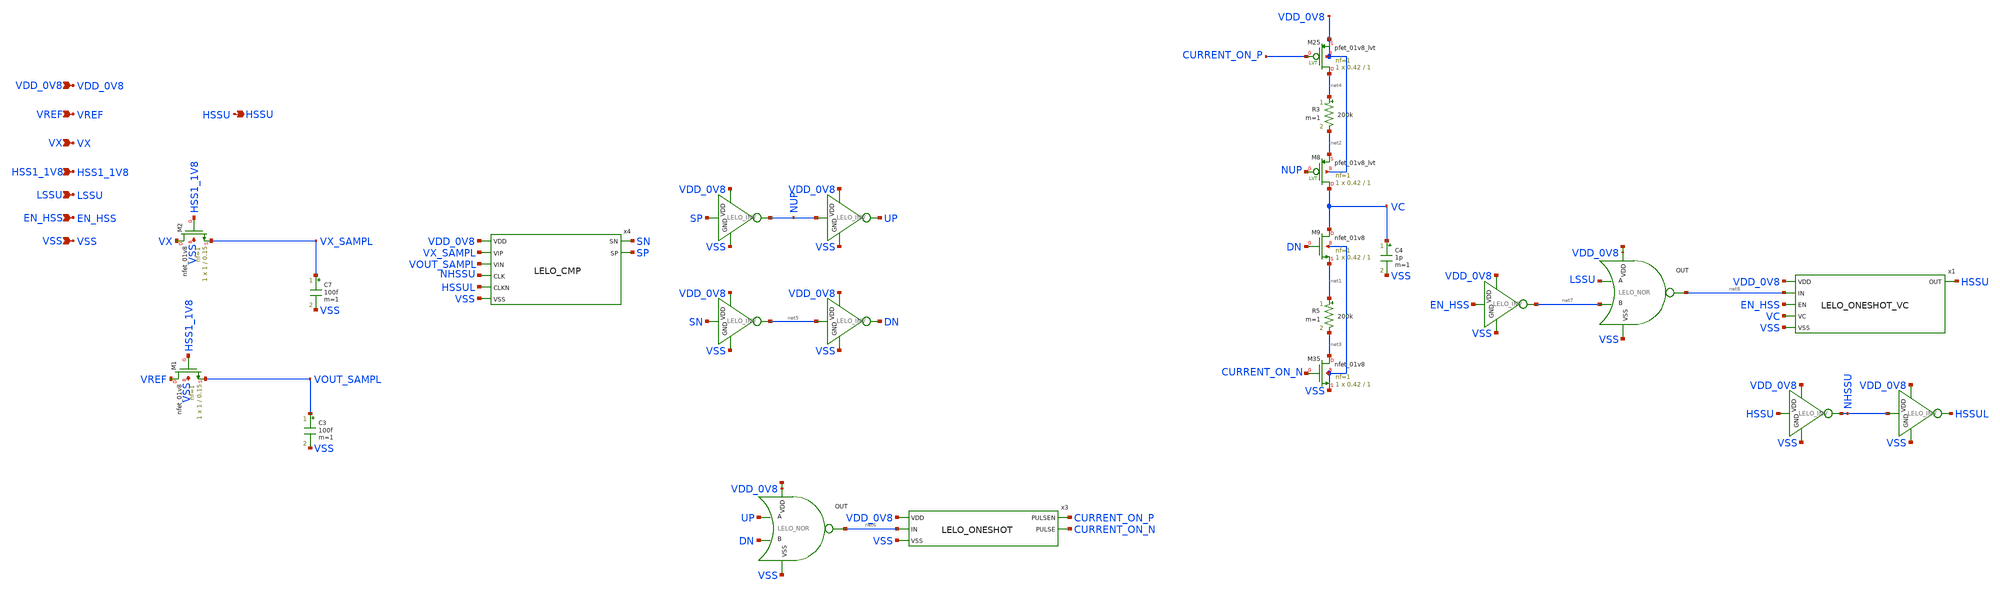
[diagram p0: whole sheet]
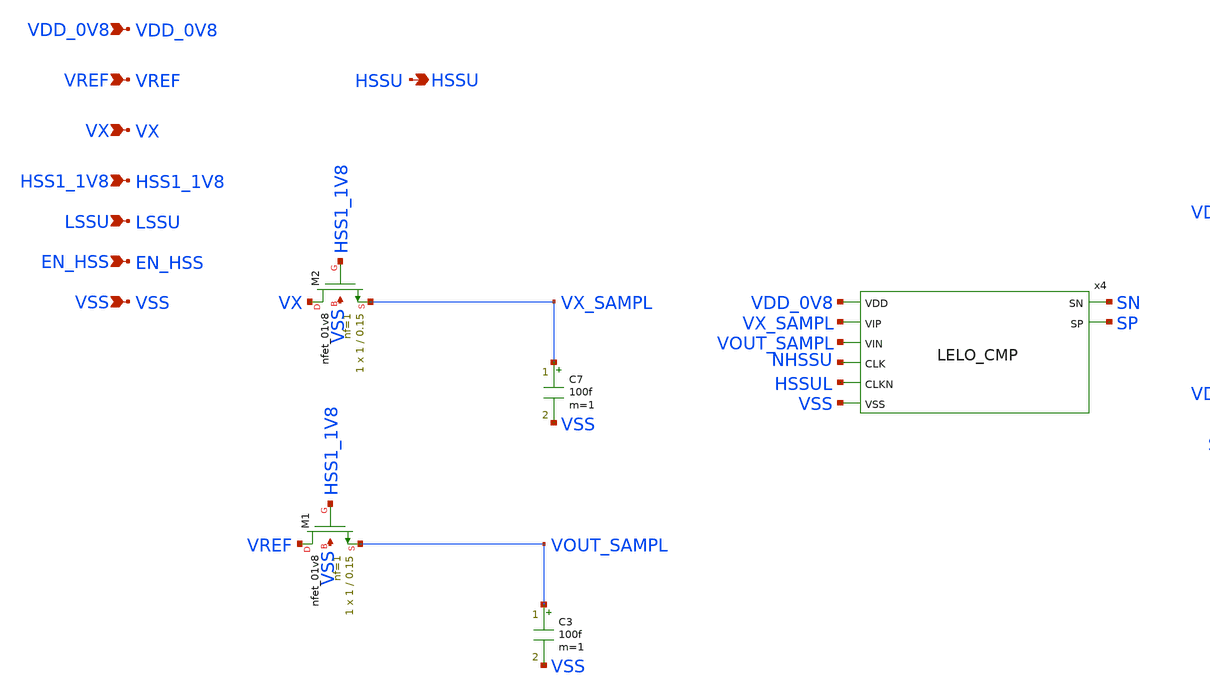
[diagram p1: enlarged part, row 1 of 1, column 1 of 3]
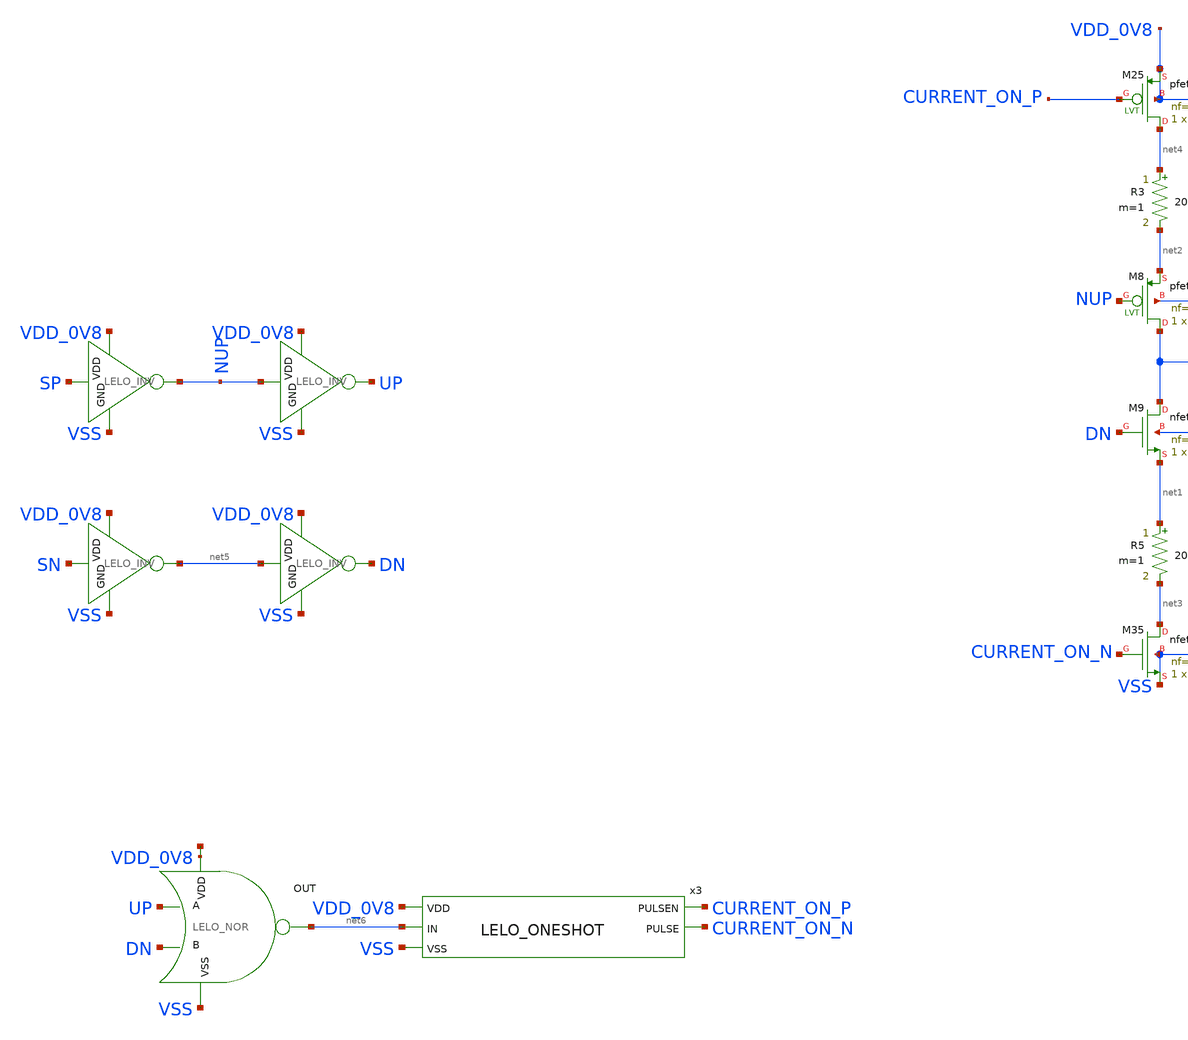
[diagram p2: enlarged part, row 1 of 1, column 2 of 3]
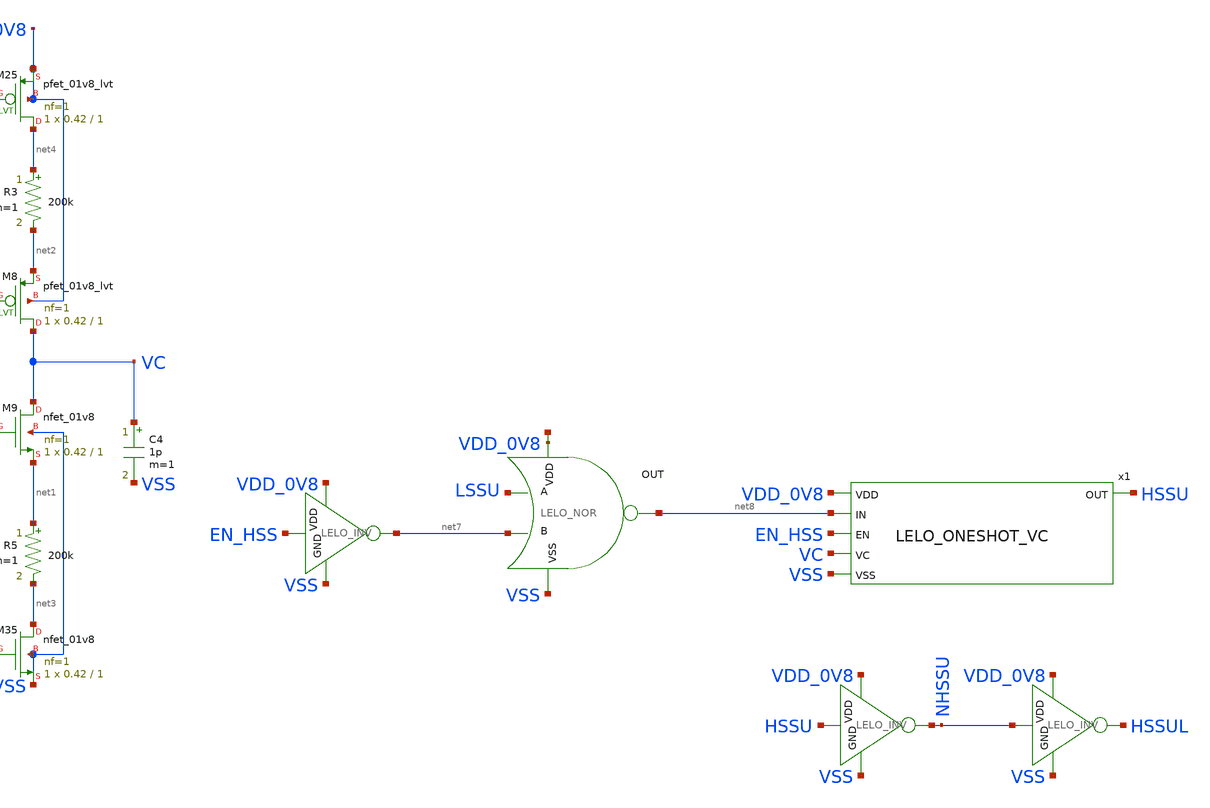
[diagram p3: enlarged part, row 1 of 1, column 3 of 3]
** sch_path: design/LELO_SVOD_SKY130A/LELO_SVOD_HSSCNTRL.sch
**.subckt LELO_SVOD_HSSCNTRL VREF HSSU VX LSSU VSS EN_HSS VDD_0V8 HSS1_1V8
*.ipin VREF
*.opin HSSU
*.ipin VX
*.ipin LSSU
*.ipin VSS
*.ipin EN_HSS
*.ipin VDD_0V8
*.ipin HSS1_1V8
C7 VX_SAMPL VSS 100f m=1
C3 VOUT_SAMPL VSS 100f m=1
x4 SN SP VDD_0V8 VX_SAMPL VOUT_SAMPL NHSSU HSSUL VSS LELO_CMP
C4 VC VSS 1p m=1
XM9 VC DN net1 VSS sky130_fd_pr__nfet_01v8 L=1 W=0.42 nf=1 ad='int((1 + 1)/2) * 0.42 / 1 * 0.29' as='int((1 + 2)/2) * 0.42 / 1 * 0.29'
+ pd='2*int((1 + 1)/2) * (0.42 / 1 + 0.29)' ps='2*int((1 + 2)/2) * (0.42 / 1 + 0.29)' nrd='0.29 / 0.42 '
+ nrs='0.29 / 0.42 ' sa=0 sb=0 sd=0 mult=1 m=1
x10 VDD_0V8 SP NUP VSS LELO_INV
R5 net1 net3 200k m=1
XM35 net3 CURRENT_ON_N VSS VSS sky130_fd_pr__nfet_01v8 L=1 W=0.42 nf=1 ad='int((1 + 1)/2) * 0.42 / 1 * 0.29'
+ as='int((1 + 2)/2) * 0.42 / 1 * 0.29' pd='2*int((1 + 1)/2) * (0.42 / 1 + 0.29)' ps='2*int((1 + 2)/2) * (0.42 / 1 + 0.29)'
+ nrd='0.29 / 0.42 ' nrs='0.29 / 0.42 ' sa=0 sb=0 sd=0 mult=1 m=1
x11 VDD_0V8 SN net5 VSS LELO_INV
x14 VDD_0V8 net5 DN VSS LELO_INV
x17 VDD_0V8 NUP UP VSS LELO_INV
x2 net9 net6 UP DN VSS LELO_NOR
x3 VDD_0V8 net6 VSS CURRENT_ON_P CURRENT_ON_N LELO_ONESHOT
R3 net4 net2 200k m=1
XM8 VC NUP net2 VDD_0V8 sky130_fd_pr__pfet_01v8_lvt L=1 W=0.42 nf=1 ad='int((1 + 1)/2) * 0.42 / 1 * 0.29'
+ as='int((1 + 2)/2) * 0.42 / 1 * 0.29' pd='2*int((1 + 1)/2) * (0.42 / 1 + 0.29)' ps='2*int((1 + 2)/2) * (0.42 / 1 + 0.29)'
+ nrd='0.29 / 0.42 ' nrs='0.29 / 0.42 ' sa=0 sb=0 sd=0 mult=1 m=1
XM25 net4 CURRENT_ON_P VDD_0V8 VDD_0V8 sky130_fd_pr__pfet_01v8_lvt L=1 W=0.42 nf=1 ad='int((1 + 1)/2) * 0.42 / 1 * 0.29'
+ as='int((1 + 2)/2) * 0.42 / 1 * 0.29' pd='2*int((1 + 1)/2) * (0.42 / 1 + 0.29)' ps='2*int((1 + 2)/2) * (0.42 / 1 + 0.29)'
+ nrd='0.29 / 0.42 ' nrs='0.29 / 0.42 ' sa=0 sb=0 sd=0 mult=1 m=1
x1 VDD_0V8 net8 EN_HSS HSSU VC VSS LELO_ONESHOT_VC
x5 net10 net8 LSSU net7 VSS LELO_NOR
x6 VDD_0V8 EN_HSS net7 VSS LELO_INV
x7 VDD_0V8 HSSU NHSSU VSS LELO_INV
x8 VDD_0V8 NHSSU HSSUL VSS LELO_INV
XM1 VREF HSS1_1V8 VOUT_SAMPL VSS sky130_fd_pr__nfet_01v8 L=0.15 W=1 nf=1 ad='int((1 + 1)/2) * 1 / 1 * 0.29'
+ as='int((1 + 2)/2) * 1 / 1 * 0.29' pd='2*int((1 + 1)/2) * (1 / 1 + 0.29)' ps='2*int((1 + 2)/2) * (1 / 1 + 0.29)'
+ nrd='0.29 / 1 ' nrs='0.29 / 1 ' sa=0 sb=0 sd=0 mult=1 m=1
XM2 VX HSS1_1V8 VX_SAMPL VSS sky130_fd_pr__nfet_01v8 L=0.15 W=1 nf=1 ad='int((1 + 1)/2) * 1 / 1 * 0.29'
+ as='int((1 + 2)/2) * 1 / 1 * 0.29' pd='2*int((1 + 1)/2) * (1 / 1 + 0.29)' ps='2*int((1 + 2)/2) * (1 / 1 + 0.29)'
+ nrd='0.29 / 1 ' nrs='0.29 / 1 ' sa=0 sb=0 sd=0 mult=1 m=1
**.ends

* expanding   symbol:  LELO_SVOD_SKY130A/LELO_CMP.sym # of pins=8
** sym_path: design/LELO_SVOD_SKY130A/LELO_CMP.sym
** sch_path: design/LELO_SVOD_SKY130A/LELO_CMP.sch
.subckt LELO_CMP SN SP VDD VIP VIN CLK CLKN VSS
*.ipin VIP
*.ipin VIN
*.ipin CLK
*.ipin CLKN
*.ipin VDD
*.ipin VSS
*.opin SN
*.opin SP
XM2 SN net3 net5 VDD sky130_fd_pr__pfet_01v8_lvt L=0.44 W=1.92 nf=2 ad='int((2 + 1)/2) * 1.92 / 2 * 0.29'
+ as='int((2 + 2)/2) * 1.92 / 2 * 0.29' pd='2*int((2 + 1)/2) * (1.92 / 2 + 0.29)' ps='2*int((2 + 2)/2) * (1.92 / 2 + 0.29)'
+ nrd='0.29 / 1.92 ' nrs='0.29 / 1.92 ' sa=0 sb=0 sd=0 mult=3 m=3
XM1 SP net2 net6 VDD sky130_fd_pr__pfet_01v8_lvt L=0.44 W=1.92 nf=2 ad='int((2 + 1)/2) * 1.92 / 2 * 0.29'
+ as='int((2 + 2)/2) * 1.92 / 2 * 0.29' pd='2*int((2 + 1)/2) * (1.92 / 2 + 0.29)' ps='2*int((2 + 2)/2) * (1.92 / 2 + 0.29)'
+ nrd='0.29 / 1.92 ' nrs='0.29 / 1.92 ' sa=0 sb=0 sd=0 mult=3 m=3
XM3 net2 VIP net1 VSS sky130_fd_pr__nfet_01v8_lvt L=0.44 W=6.4 nf=1 ad='int((1 + 1)/2) * 6.4 / 1 * 0.29'
+ as='int((1 + 2)/2) * 6.4 / 1 * 0.29' pd='2*int((1 + 1)/2) * (6.4 / 1 + 0.29)' ps='2*int((1 + 2)/2) * (6.4 / 1 + 0.29)'
+ nrd='0.29 / 6.4 ' nrs='0.29 / 6.4 ' sa=0 sb=0 sd=0 mult=1 m=1
XM4 net3 VIN net1 VSS sky130_fd_pr__nfet_01v8_lvt L=0.44 W=6.4 nf=1 ad='int((1 + 1)/2) * 6.4 / 1 * 0.29'
+ as='int((1 + 2)/2) * 6.4 / 1 * 0.29' pd='2*int((1 + 1)/2) * (6.4 / 1 + 0.29)' ps='2*int((1 + 2)/2) * (6.4 / 1 + 0.29)'
+ nrd='0.29 / 6.4 ' nrs='0.29 / 6.4 ' sa=0 sb=0 sd=0 mult=1 m=1
XM5 net3 CLK VDD VDD sky130_fd_pr__pfet_01v8_lvt L=0.94 W=1.92 nf=2 ad='int((2 + 1)/2) * 1.92 / 2 * 0.29'
+ as='int((2 + 2)/2) * 1.92 / 2 * 0.29' pd='2*int((2 + 1)/2) * (1.92 / 2 + 0.29)' ps='2*int((2 + 2)/2) * (1.92 / 2 + 0.29)'
+ nrd='0.29 / 1.92 ' nrs='0.29 / 1.92 ' sa=0 sb=0 sd=0 mult=1 m=1
XM6 net6 SN VDD VDD sky130_fd_pr__pfet_01v8_lvt L=0.94 W=1.92 nf=2 ad='int((2 + 1)/2) * 1.92 / 2 * 0.29'
+ as='int((2 + 2)/2) * 1.92 / 2 * 0.29' pd='2*int((2 + 1)/2) * (1.92 / 2 + 0.29)' ps='2*int((2 + 2)/2) * (1.92 / 2 + 0.29)'
+ nrd='0.29 / 1.92 ' nrs='0.29 / 1.92 ' sa=0 sb=0 sd=0 mult=1 m=1
XM7 net5 SP VDD VDD sky130_fd_pr__pfet_01v8_lvt L=0.94 W=1.92 nf=2 ad='int((2 + 1)/2) * 1.92 / 2 * 0.29'
+ as='int((2 + 2)/2) * 1.92 / 2 * 0.29' pd='2*int((2 + 1)/2) * (1.92 / 2 + 0.29)' ps='2*int((2 + 2)/2) * (1.92 / 2 + 0.29)'
+ nrd='0.29 / 1.92 ' nrs='0.29 / 1.92 ' sa=0 sb=0 sd=0 mult=1 m=1
XM8 net2 CLK VDD VDD sky130_fd_pr__pfet_01v8_lvt L=0.94 W=1.92 nf=2 ad='int((2 + 1)/2) * 1.92 / 2 * 0.29'
+ as='int((2 + 2)/2) * 1.92 / 2 * 0.29' pd='2*int((2 + 1)/2) * (1.92 / 2 + 0.29)' ps='2*int((2 + 2)/2) * (1.92 / 2 + 0.29)'
+ nrd='0.29 / 1.92 ' nrs='0.29 / 1.92 ' sa=0 sb=0 sd=0 mult=1 m=1
XM9 net1 CLK net4 VSS sky130_fd_pr__nfet_01v8 L=0.94 W=1.92 nf=2 ad='int((2 + 1)/2) * 1.92 / 2 * 0.29'
+ as='int((2 + 2)/2) * 1.92 / 2 * 0.29' pd='2*int((2 + 1)/2) * (1.92 / 2 + 0.29)' ps='2*int((2 + 2)/2) * (1.92 / 2 + 0.29)'
+ nrd='0.29 / 1.92 ' nrs='0.29 / 1.92 ' sa=0 sb=0 sd=0 mult=1 m=1
XM10 net4 CLK VSS VSS sky130_fd_pr__nfet_01v8 L=0.94 W=1.92 nf=2 ad='int((2 + 1)/2) * 1.92 / 2 * 0.29'
+ as='int((2 + 2)/2) * 1.92 / 2 * 0.29' pd='2*int((2 + 1)/2) * (1.92 / 2 + 0.29)' ps='2*int((2 + 2)/2) * (1.92 / 2 + 0.29)'
+ nrd='0.29 / 1.92 ' nrs='0.29 / 1.92 ' sa=0 sb=0 sd=0 mult=1 m=1
XM11 SN CLKN VSS VSS sky130_fd_pr__nfet_01v8 L=0.94 W=1.92 nf=2 ad='int((2 + 1)/2) * 1.92 / 2 * 0.29'
+ as='int((2 + 2)/2) * 1.92 / 2 * 0.29' pd='2*int((2 + 1)/2) * (1.92 / 2 + 0.29)' ps='2*int((2 + 2)/2) * (1.92 / 2 + 0.29)'
+ nrd='0.29 / 1.92 ' nrs='0.29 / 1.92 ' sa=0 sb=0 sd=0 mult=1 m=1
XM12 SP SN VSS VSS sky130_fd_pr__nfet_01v8 L=0.94 W=1.92 nf=2 ad='int((2 + 1)/2) * 1.92 / 2 * 0.29' as='int((2 + 2)/2) * 1.92 / 2 * 0.29'
+ pd='2*int((2 + 1)/2) * (1.92 / 2 + 0.29)' ps='2*int((2 + 2)/2) * (1.92 / 2 + 0.29)' nrd='0.29 / 1.92 '
+ nrs='0.29 / 1.92 ' sa=0 sb=0 sd=0 mult=1 m=1
XM13 SN SP VSS VSS sky130_fd_pr__nfet_01v8 L=0.94 W=1.92 nf=2 ad='int((2 + 1)/2) * 1.92 / 2 * 0.29' as='int((2 + 2)/2) * 1.92 / 2 * 0.29'
+ pd='2*int((2 + 1)/2) * (1.92 / 2 + 0.29)' ps='2*int((2 + 2)/2) * (1.92 / 2 + 0.29)' nrd='0.29 / 1.92 '
+ nrs='0.29 / 1.92 ' sa=0 sb=0 sd=0 mult=1 m=1
XM14 SP CLKN VSS VSS sky130_fd_pr__nfet_01v8 L=0.94 W=1.92 nf=2 ad='int((2 + 1)/2) * 1.92 / 2 * 0.29'
+ as='int((2 + 2)/2) * 1.92 / 2 * 0.29' pd='2*int((2 + 1)/2) * (1.92 / 2 + 0.29)' ps='2*int((2 + 2)/2) * (1.92 / 2 + 0.29)'
+ nrd='0.29 / 1.92 ' nrs='0.29 / 1.92 ' sa=0 sb=0 sd=0 mult=1 m=1
.ends


* expanding   symbol:  LELO_SVOD_SKY130A/LELO_INV.sym # of pins=4
** sym_path: design/LELO_SVOD_SKY130A/LELO_INV.sym
** sch_path: design/LELO_SVOD_SKY130A/LELO_INV.sch
.subckt LELO_INV VDD VIN VOUT GND
*.ipin VIN
*.ipin VDD
*.ipin GND
*.opin VOUT
XM1 VOUT VIN GND GND sky130_fd_pr__nfet_01v8_lvt L=0.15 W=1 nf=1 ad='int((1 + 1)/2) * 1 / 1 * 0.29' as='int((1 + 2)/2) * 1 / 1 * 0.29'
+ pd='2*int((1 + 1)/2) * (1 / 1 + 0.29)' ps='2*int((1 + 2)/2) * (1 / 1 + 0.29)' nrd='0.29 / 1 ' nrs='0.29 / 1 '
+ sa=0 sb=0 sd=0 mult=1 m=1
XM2 VOUT VIN VDD VDD sky130_fd_pr__pfet_01v8_lvt L=0.35 W=1 nf=1 ad='int((1 + 1)/2) * 1 / 1 * 0.29' as='int((1 + 2)/2) * 1 / 1 * 0.29'
+ pd='2*int((1 + 1)/2) * (1 / 1 + 0.29)' ps='2*int((1 + 2)/2) * (1 / 1 + 0.29)' nrd='0.29 / 1 ' nrs='0.29 / 1 '
+ sa=0 sb=0 sd=0 mult=2 m=2
.ends


* expanding   symbol:  LELO_SVOD_SKY130A/LELO_NOR.sym # of pins=5
** sym_path: design/LELO_SVOD_SKY130A/LELO_NOR.sym
** sch_path: design/LELO_SVOD_SKY130A/LELO_NOR.sch
.subckt LELO_NOR VDD OUT A B VSS
*.ipin VDD
*.ipin VSS
*.opin OUT
*.ipin A
*.ipin B
XM2 OUT B VSS VSS sky130_fd_pr__nfet_01v8 L=0.15 W=2 nf=1 ad='int((1 + 1)/2) * 2 / 1 * 0.29' as='int((1 + 2)/2) * 2 / 1 * 0.29'
+ pd='2*int((1 + 1)/2) * (2 / 1 + 0.29)' ps='2*int((1 + 2)/2) * (2 / 1 + 0.29)' nrd='0.29 / 2 ' nrs='0.29 / 2 '
+ sa=0 sb=0 sd=0 mult=1 m=1
XM1 OUT A VSS VSS sky130_fd_pr__nfet_01v8 L=0.15 W=2 nf=1 ad='int((1 + 1)/2) * 2 / 1 * 0.29' as='int((1 + 2)/2) * 2 / 1 * 0.29'
+ pd='2*int((1 + 1)/2) * (2 / 1 + 0.29)' ps='2*int((1 + 2)/2) * (2 / 1 + 0.29)' nrd='0.29 / 2 ' nrs='0.29 / 2 '
+ sa=0 sb=0 sd=0 mult=1 m=1
XM3 OUT B net1 VDD sky130_fd_pr__pfet_01v8 L=0.15 W=4 nf=1 ad='int((1 + 1)/2) * 4 / 1 * 0.29' as='int((1 + 2)/2) * 4 / 1 * 0.29'
+ pd='2*int((1 + 1)/2) * (4 / 1 + 0.29)' ps='2*int((1 + 2)/2) * (4 / 1 + 0.29)' nrd='0.29 / 4 ' nrs='0.29 / 4 '
+ sa=0 sb=0 sd=0 mult=1 m=1
XM4 net1 A VDD VDD sky130_fd_pr__pfet_01v8 L=0.15 W=4 nf=1 ad='int((1 + 1)/2) * 4 / 1 * 0.29' as='int((1 + 2)/2) * 4 / 1 * 0.29'
+ pd='2*int((1 + 1)/2) * (4 / 1 + 0.29)' ps='2*int((1 + 2)/2) * (4 / 1 + 0.29)' nrd='0.29 / 4 ' nrs='0.29 / 4 '
+ sa=0 sb=0 sd=0 mult=1 m=1
.ends


* expanding   symbol:  LELO_SVOD_SKY130A/LELO_ONESHOT.sym # of pins=5
** sym_path: design/LELO_SVOD_SKY130A/LELO_ONESHOT.sym
** sch_path: design/LELO_SVOD_SKY130A/LELO_ONESHOT.sch
.subckt LELO_ONESHOT VDD IN VSS PULSEN PULSE
*.ipin VDD
*.ipin IN
*.ipin VSS
*.opin PULSEN
*.opin PULSE
x8 VDD PULSE PULSEN VSS LELO_INV
x12 VDD net3 net1 PULSE VSS LELO_NOR
C6 net2 net3 100f m=1
x13 VDD net2 PULSE VSS LELO_INV
x18 VDD IN net1 VSS LELO_INV
XM1 net2 0 VDD VDD sky130_fd_pr__pfet_01v8_lvt L=1 W=0.42 nf=1 ad='int((1 + 1)/2) * 0.42 / 1 * 0.29'
+ as='int((1 + 2)/2) * 0.42 / 1 * 0.29' pd='2*int((1 + 1)/2) * (0.42 / 1 + 0.29)' ps='2*int((1 + 2)/2) * (0.42 / 1 + 0.29)'
+ nrd='0.29 / 0.42 ' nrs='0.29 / 0.42 ' sa=0 sb=0 sd=0 mult=1 m=1
.ends


* expanding   symbol:  LELO_SVOD_SKY130A/LELO_ONESHOT_VC.sym # of pins=6
** sym_path: design/LELO_SVOD_SKY130A/LELO_ONESHOT_VC.sym
** sch_path: design/LELO_SVOD_SKY130A/LELO_ONESHOT_VC.sch
.subckt LELO_ONESHOT_VC VDD IN EN OUT VC VSS
*.ipin VDD
*.ipin IN
*.ipin VC
*.ipin VSS
*.opin OUT
*.ipin EN
x2 net3 net2 IN OUT VSS LELO_NOR
C5 net1 net2 20f m=1
x3 VDD net1 OUT VSS LELO_INV
XM4 net1 VC VDD VDD sky130_fd_pr__pfet_01v8_lvt L=10 W=0.42 nf=1 ad='int((1 + 1)/2) * 0.42 / 1 * 0.29'
+ as='int((1 + 2)/2) * 0.42 / 1 * 0.29' pd='2*int((1 + 1)/2) * (0.42 / 1 + 0.29)' ps='2*int((1 + 2)/2) * (0.42 / 1 + 0.29)'
+ nrd='0.29 / 0.42 ' nrs='0.29 / 0.42 ' sa=0 sb=0 sd=0 mult=1 m=1
XM1 net1 VSS VDD VDD sky130_fd_pr__pfet_01v8 L=1 W=0.42 nf=1 ad='int((1 + 1)/2) * 0.42 / 1 * 0.29' as='int((1 + 2)/2) * 0.42 / 1 * 0.29'
+ pd='2*int((1 + 1)/2) * (0.42 / 1 + 0.29)' ps='2*int((1 + 2)/2) * (0.42 / 1 + 0.29)' nrd='0.29 / 0.42 '
+ nrs='0.29 / 0.42 ' sa=0 sb=0 sd=0 mult=1 m=1
XM2 net1 EN VDD VDD sky130_fd_pr__pfet_01v8 L=0.15 W=1 nf=1 ad='int((1 + 1)/2) * 1 / 1 * 0.29' as='int((1 + 2)/2) * 1 / 1 * 0.29'
+ pd='2*int((1 + 1)/2) * (1 / 1 + 0.29)' ps='2*int((1 + 2)/2) * (1 / 1 + 0.29)' nrd='0.29 / 1 ' nrs='0.29 / 1 '
+ sa=0 sb=0 sd=0 mult=10 m=10
.ends

.end
